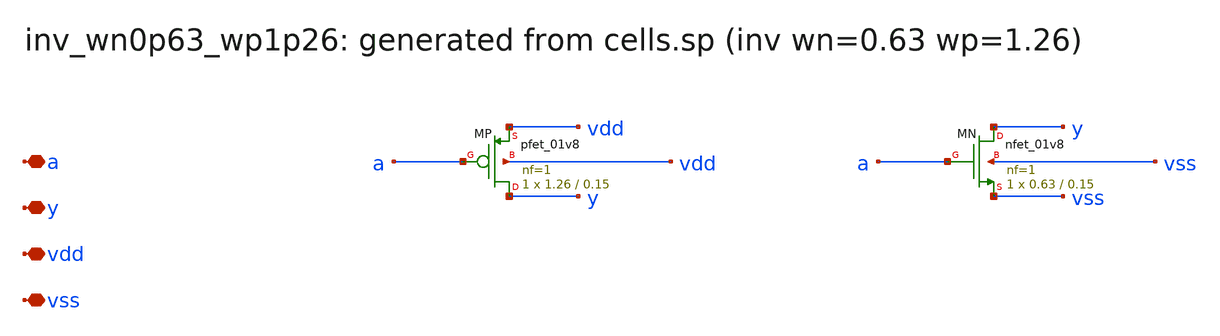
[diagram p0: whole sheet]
** sch_path: sram/xschem/inv_wn0p63_wp1p26.sch
**.subckt inv_wn0p63_wp1p26 a y vdd vss
*.iopin a
*.iopin y
*.iopin vdd
*.iopin vss
XMP y a vdd vdd sky130_fd_pr__pfet_01v8 L=0.15 W=1.26 nf=1 ad='int((nf+1)/2) * W/nf * 0.29' as='int((nf+2)/2) * W/nf * 0.29'
+ pd='2*int((nf+1)/2) * (W/nf + 0.29)' ps='2*int((nf+2)/2) * (W/nf + 0.29)' nrd='0.29 / W' nrs='0.29 / W'
+ sa=0 sb=0 sd=0 mult=1 m=1
XMN y a vss vss sky130_fd_pr__nfet_01v8 L=0.15 W=0.63 nf=1 ad='int((1 + 1)/2) * 0.63 / 1 * 0.29' as='int((1 + 2)/2) * 0.63 / 1 * 0.29'
+ pd='2*int((1 + 1)/2) * (0.63 / 1 + 0.29)' ps='2*int((1 + 2)/2) * (0.63 / 1 + 0.29)' nrd='0.29 / 0.63 '
+ nrs='0.29 / 0.63 ' sa=0 sb=0 sd=0 mult=1 m=1
**.ends
.end
